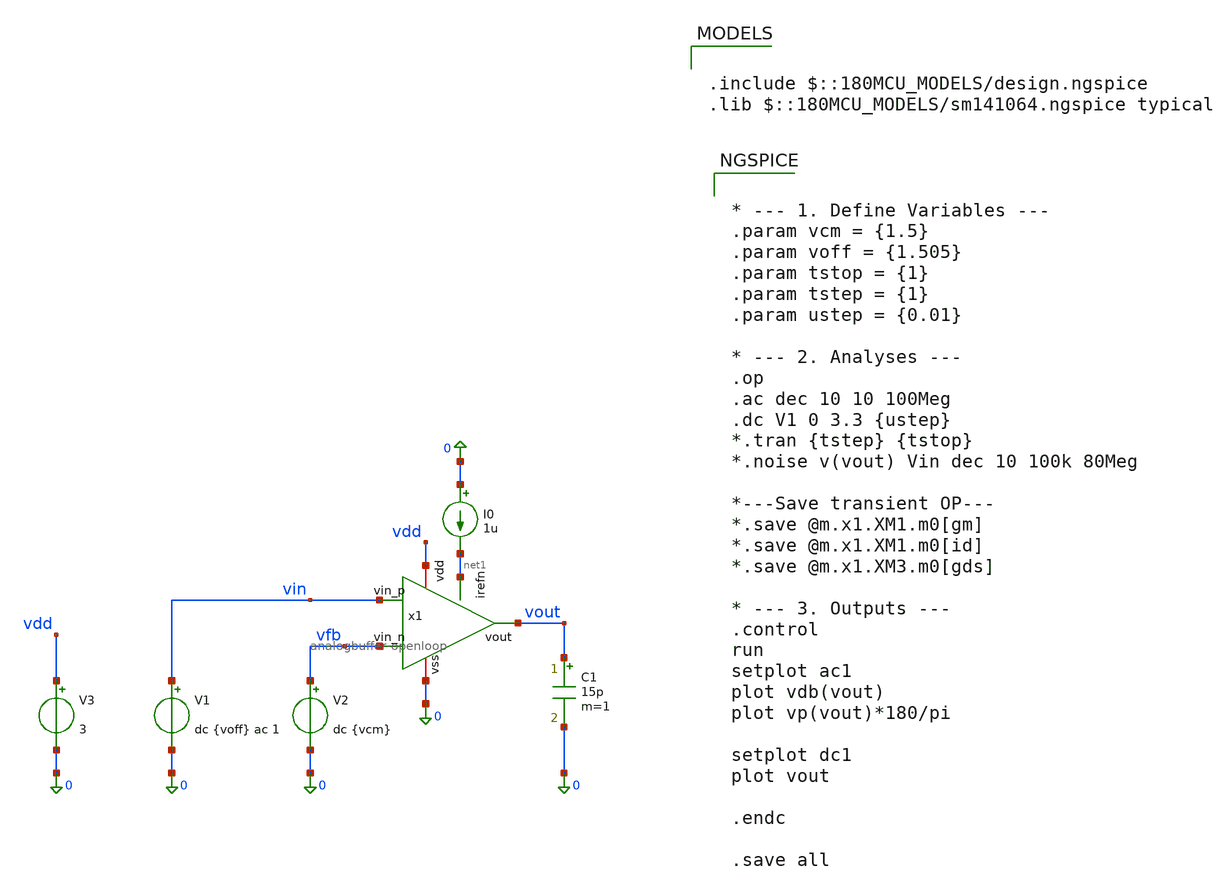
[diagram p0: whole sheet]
** sch_path: Tobias/2026 07 17 Results/analogbuffer/analogbuffer-openloop-tb.sch
**.subckt analogbuffer-openloop-tb
x1 vdd net1 vin vout vfb 0 analogbuffer-openloop
V1 vin 0 dc {voff} ac 1
V2 vfb 0 dc {vcm}
C1 vout 0 15p m=1
I0 0 net1 1u
V3 vdd 0 3
**** begin user architecture code


* --- 1. Define Variables ---
.param vcm = {1.5}
.param voff = {1.505}
.param tstop = {1}
.param tstep = {1}
.param ustep = {0.01}

* --- 2. Analyses ---
.op
.ac dec 10 10 100Meg
.dc V1 0 3.3 {ustep}
*.tran {tstep} {tstop}
*.noise v(vout) Vin dec 10 100k 80Meg

*---Save transient OP---
*.save @m.x1.XM1.m0[gm]
*.save @m.x1.XM1.m0[id]
*.save @m.x1.XM3.m0[gds]

* --- 3. Outputs ---
.control
run
setplot ac1
plot vdb(vout)
plot vp(vout)*180/pi

setplot dc1
plot vout

.endc

.save all



.include $::180MCU_MODELS/design.ngspice
.lib $::180MCU_MODELS/sm141064.ngspice typical

**** end user architecture code
**.ends

* expanding   symbol:  analogbuffer/analogbuffer-openloop.sym # of pins=6
** sym_path: Tobias/2026 07 17 Results/analogbuffer/analogbuffer-openloop.sym
** sch_path: Tobias/2026 07 17 Results/analogbuffer/analogbuffer-openloop.sch
.subckt analogbuffer-openloop vdd irefn vin_p vout vin_n vss
*.iopin vdd
*.iopin vss
*.ipin vin_p
*.opin vout
*.ipin irefn
*.ipin vin_n
XM2P net7 vin_p net10 vdd pfet_03v3 L=4u W=80u nf=1 ad='int((nf+1)/2) * W/nf * 0.18u' as='int((nf+2)/2) * W/nf * 0.18u'
+ pd='2*int((nf+1)/2) * (W/nf + 0.18u)' ps='2*int((nf+2)/2) * (W/nf + 0.18u)' nrd='0.18u / W' nrs='0.18u / W'
+ sa=0 sb=0 sd=0 m=1
XM2N net1 vin_p net4 vss nfet_03v3 L=4u W=40u nf=1 ad='int((nf+1)/2) * W/nf * 0.18u' as='int((nf+2)/2) * W/nf * 0.18u'
+ pd='2*int((nf+1)/2) * (W/nf + 0.18u)' ps='2*int((nf+2)/2) * (W/nf + 0.18u)' nrd='0.18u / W' nrs='0.18u / W'
+ sa=0 sb=0 sd=0 m=1
XM3N net4 net8 vss vss nfet_03v3 L=4u W=2u nf=1 ad='int((nf+1)/2) * W/nf * 0.18u' as='int((nf+2)/2) * W/nf * 0.18u'
+ pd='2*int((nf+1)/2) * (W/nf + 0.18u)' ps='2*int((nf+2)/2) * (W/nf + 0.18u)' nrd='0.18u / W' nrs='0.18u / W'
+ sa=0 sb=0 sd=0 m=1
XM1NR net3 vin_n net4 vss nfet_03v3 L=4u W=40u nf=1 ad='int((nf+1)/2) * W/nf * 0.18u' as='int((nf+2)/2) * W/nf * 0.18u'
+ pd='2*int((nf+1)/2) * (W/nf + 0.18u)' ps='2*int((nf+2)/2) * (W/nf + 0.18u)' nrd='0.18u / W' nrs='0.18u / W'
+ sa=0 sb=0 sd=0 m=1
XM2NR net3 net3 vdd vdd pfet_03v3 L=2u W=4u nf=1 ad='int((nf+1)/2) * W/nf * 0.18u' as='int((nf+2)/2) * W/nf * 0.18u'
+ pd='2*int((nf+1)/2) * (W/nf + 0.18u)' ps='2*int((nf+2)/2) * (W/nf + 0.18u)' nrd='0.18u / W' nrs='0.18u / W'
+ sa=0 sb=0 sd=0 m=1
XM3NR net2 net3 vdd vdd pfet_03v3 L=2u W=4u nf=1 ad='int((nf+1)/2) * W/nf * 0.18u' as='int((nf+2)/2) * W/nf * 0.18u'
+ pd='2*int((nf+1)/2) * (W/nf + 0.18u)' ps='2*int((nf+2)/2) * (W/nf + 0.18u)' nrd='0.18u / W' nrs='0.18u / W'
+ sa=0 sb=0 sd=0 m=1
XM4NR net2 net2 vdd vdd pfet_03v3 L=2u W=4u nf=1 ad='int((nf+1)/2) * W/nf * 0.18u' as='int((nf+2)/2) * W/nf * 0.18u'
+ pd='2*int((nf+1)/2) * (W/nf + 0.18u)' ps='2*int((nf+2)/2) * (W/nf + 0.18u)' nrd='0.18u / W' nrs='0.18u / W'
+ sa=0 sb=0 sd=0 m=1
XM5NR vout net2 vdd vdd pfet_03v3 L=2u W=40u nf=1 ad='int((nf+1)/2) * W/nf * 0.18u' as='int((nf+2)/2) * W/nf * 0.18u'
+ pd='2*int((nf+1)/2) * (W/nf + 0.18u)' ps='2*int((nf+2)/2) * (W/nf + 0.18u)' nrd='0.18u / W' nrs='0.18u / W'
+ sa=0 sb=0 sd=0 m=1
XM5N vout net1 vdd vdd pfet_03v3 L=2u W=40u nf=1 ad='int((nf+1)/2) * W/nf * 0.18u' as='int((nf+2)/2) * W/nf * 0.18u'
+ pd='2*int((nf+1)/2) * (W/nf + 0.18u)' ps='2*int((nf+2)/2) * (W/nf + 0.18u)' nrd='0.18u / W' nrs='0.18u / W'
+ sa=0 sb=0 sd=0 m=1
XM4N net1 net1 vdd vdd pfet_03v3 L=2u W=4u nf=1 ad='int((nf+1)/2) * W/nf * 0.18u' as='int((nf+2)/2) * W/nf * 0.18u'
+ pd='2*int((nf+1)/2) * (W/nf + 0.18u)' ps='2*int((nf+2)/2) * (W/nf + 0.18u)' nrd='0.18u / W' nrs='0.18u / W'
+ sa=0 sb=0 sd=0 m=1
XM5NS net2 irefn vss vss nfet_03v3 L=2u W=2u nf=1 ad='int((nf+1)/2) * W/nf * 0.18u' as='int((nf+2)/2) * W/nf * 0.18u'
+ pd='2*int((nf+1)/2) * (W/nf + 0.18u)' ps='2*int((nf+2)/2) * (W/nf + 0.18u)' nrd='0.18u / W' nrs='0.18u / W'
+ sa=0 sb=0 sd=0 m=1
XM1PR net5 vin_n net10 vdd pfet_03v3 L=4u W=80u nf=1 ad='int((nf+1)/2) * W/nf * 0.18u' as='int((nf+2)/2) * W/nf * 0.18u'
+ pd='2*int((nf+1)/2) * (W/nf + 0.18u)' ps='2*int((nf+2)/2) * (W/nf + 0.18u)' nrd='0.18u / W' nrs='0.18u / W'
+ sa=0 sb=0 sd=0 m=1
XM3P net10 net9 vdd vdd pfet_03v3 L=4u W=4u nf=1 ad='int((nf+1)/2) * W/nf * 0.18u' as='int((nf+2)/2) * W/nf * 0.18u'
+ pd='2*int((nf+1)/2) * (W/nf + 0.18u)' ps='2*int((nf+2)/2) * (W/nf + 0.18u)' nrd='0.18u / W' nrs='0.18u / W'
+ sa=0 sb=0 sd=0 m=1
XM2PR net5 net5 vss vss nfet_03v3 L=2u W=2u nf=1 ad='int((nf+1)/2) * W/nf * 0.18u' as='int((nf+2)/2) * W/nf * 0.18u'
+ pd='2*int((nf+1)/2) * (W/nf + 0.18u)' ps='2*int((nf+2)/2) * (W/nf + 0.18u)' nrd='0.18u / W' nrs='0.18u / W'
+ sa=0 sb=0 sd=0 m=1
XM3PR net6 net5 vss vss nfet_03v3 L=2u W=2u nf=1 ad='int((nf+1)/2) * W/nf * 0.18u' as='int((nf+2)/2) * W/nf * 0.18u'
+ pd='2*int((nf+1)/2) * (W/nf + 0.18u)' ps='2*int((nf+2)/2) * (W/nf + 0.18u)' nrd='0.18u / W' nrs='0.18u / W'
+ sa=0 sb=0 sd=0 m=1
XM4PR net6 net6 vss vss nfet_03v3 L=2u W=2u nf=1 ad='int((nf+1)/2) * W/nf * 0.18u' as='int((nf+2)/2) * W/nf * 0.18u'
+ pd='2*int((nf+1)/2) * (W/nf + 0.18u)' ps='2*int((nf+2)/2) * (W/nf + 0.18u)' nrd='0.18u / W' nrs='0.18u / W'
+ sa=0 sb=0 sd=0 m=1
XM5PR vout net6 vss vss nfet_03v3 L=2u W=20u nf=1 ad='int((nf+1)/2) * W/nf * 0.18u' as='int((nf+2)/2) * W/nf * 0.18u'
+ pd='2*int((nf+1)/2) * (W/nf + 0.18u)' ps='2*int((nf+2)/2) * (W/nf + 0.18u)' nrd='0.18u / W' nrs='0.18u / W'
+ sa=0 sb=0 sd=0 m=1
XM5PS net6 irefp vdd vdd pfet_03v3 L=2u W=4u nf=1 ad='int((nf+1)/2) * W/nf * 0.18u' as='int((nf+2)/2) * W/nf * 0.18u'
+ pd='2*int((nf+1)/2) * (W/nf + 0.18u)' ps='2*int((nf+2)/2) * (W/nf + 0.18u)' nrd='0.18u / W' nrs='0.18u / W'
+ sa=0 sb=0 sd=0 m=1
XM5P vout net7 vss vss nfet_03v3 L=2u W=20u nf=1 ad='int((nf+1)/2) * W/nf * 0.18u' as='int((nf+2)/2) * W/nf * 0.18u'
+ pd='2*int((nf+1)/2) * (W/nf + 0.18u)' ps='2*int((nf+2)/2) * (W/nf + 0.18u)' nrd='0.18u / W' nrs='0.18u / W'
+ sa=0 sb=0 sd=0 m=1
XM4P net7 net7 vss vss nfet_03v3 L=2u W=2u nf=1 ad='int((nf+1)/2) * W/nf * 0.18u' as='int((nf+2)/2) * W/nf * 0.18u'
+ pd='2*int((nf+1)/2) * (W/nf + 0.18u)' ps='2*int((nf+2)/2) * (W/nf + 0.18u)' nrd='0.18u / W' nrs='0.18u / W'
+ sa=0 sb=0 sd=0 m=1
XM2NS irefp irefn vss vss nfet_03v3 L=2u W=1u nf=1 ad='int((nf+1)/2) * W/nf * 0.18u' as='int((nf+2)/2) * W/nf * 0.18u'
+ pd='2*int((nf+1)/2) * (W/nf + 0.18u)' ps='2*int((nf+2)/2) * (W/nf + 0.18u)' nrd='0.18u / W' nrs='0.18u / W'
+ sa=0 sb=0 sd=0 m=1
XM1NS irefn irefn vss vss nfet_03v3 L=2u W=1u nf=1 ad='int((nf+1)/2) * W/nf * 0.18u' as='int((nf+2)/2) * W/nf * 0.18u'
+ pd='2*int((nf+1)/2) * (W/nf + 0.18u)' ps='2*int((nf+2)/2) * (W/nf + 0.18u)' nrd='0.18u / W' nrs='0.18u / W'
+ sa=0 sb=0 sd=0 m=1
XM2PS irefp irefp vdd vdd pfet_03v3 L=2u W=2u nf=1 ad='int((nf+1)/2) * W/nf * 0.18u' as='int((nf+2)/2) * W/nf * 0.18u'
+ pd='2*int((nf+1)/2) * (W/nf + 0.18u)' ps='2*int((nf+2)/2) * (W/nf + 0.18u)' nrd='0.18u / W' nrs='0.18u / W'
+ sa=0 sb=0 sd=0 m=1
XMSN vdd net11 net8 vss nfet_03v3 L=2u W=2u nf=1 ad='int((nf+1)/2) * W/nf * 0.18u' as='int((nf+2)/2) * W/nf * 0.18u'
+ pd='2*int((nf+1)/2) * (W/nf + 0.18u)' ps='2*int((nf+2)/2) * (W/nf + 0.18u)' nrd='0.18u / W' nrs='0.18u / W'
+ sa=0 sb=0 sd=0 m=1
XM3NS net8 irefn vss vss nfet_03v3 L=2u W=2u nf=1 ad='int((nf+1)/2) * W/nf * 0.18u' as='int((nf+2)/2) * W/nf * 0.18u'
+ pd='2*int((nf+1)/2) * (W/nf + 0.18u)' ps='2*int((nf+2)/2) * (W/nf + 0.18u)' nrd='0.18u / W' nrs='0.18u / W'
+ sa=0 sb=0 sd=0 m=1
XM1N net11 vin_n net4 vss nfet_03v3 L=4u W=40u nf=1 ad='int((nf+1)/2) * W/nf * 0.18u' as='int((nf+2)/2) * W/nf * 0.18u'
+ pd='2*int((nf+1)/2) * (W/nf + 0.18u)' ps='2*int((nf+2)/2) * (W/nf + 0.18u)' nrd='0.18u / W' nrs='0.18u / W'
+ sa=0 sb=0 sd=0 m=1
XM4PS net11 irefp vdd vdd pfet_03v3 L=2u W=4u nf=1 ad='int((nf+1)/2) * W/nf * 0.18u' as='int((nf+2)/2) * W/nf * 0.18u'
+ pd='2*int((nf+1)/2) * (W/nf + 0.18u)' ps='2*int((nf+2)/2) * (W/nf + 0.18u)' nrd='0.18u / W' nrs='0.18u / W'
+ sa=0 sb=0 sd=0 m=1
XM3PS net9 irefp vdd vdd pfet_03v3 L=2u W=4u nf=1 ad='int((nf+1)/2) * W/nf * 0.18u' as='int((nf+2)/2) * W/nf * 0.18u'
+ pd='2*int((nf+1)/2) * (W/nf + 0.18u)' ps='2*int((nf+2)/2) * (W/nf + 0.18u)' nrd='0.18u / W' nrs='0.18u / W'
+ sa=0 sb=0 sd=0 m=1
XM1P net12 vin_n net10 vdd pfet_03v3 L=4u W=80u nf=1 ad='int((nf+1)/2) * W/nf * 0.18u' as='int((nf+2)/2) * W/nf * 0.18u'
+ pd='2*int((nf+1)/2) * (W/nf + 0.18u)' ps='2*int((nf+2)/2) * (W/nf + 0.18u)' nrd='0.18u / W' nrs='0.18u / W'
+ sa=0 sb=0 sd=0 m=1
XM4NS net12 irefn vss vss nfet_03v3 L=2u W=2u nf=1 ad='int((nf+1)/2) * W/nf * 0.18u' as='int((nf+2)/2) * W/nf * 0.18u'
+ pd='2*int((nf+1)/2) * (W/nf + 0.18u)' ps='2*int((nf+2)/2) * (W/nf + 0.18u)' nrd='0.18u / W' nrs='0.18u / W'
+ sa=0 sb=0 sd=0 m=1
XMSP vss net12 net9 vdd pfet_03v3 L=1u W=4u nf=1 ad='int((nf+1)/2) * W/nf * 0.18u' as='int((nf+2)/2) * W/nf * 0.18u'
+ pd='2*int((nf+1)/2) * (W/nf + 0.18u)' ps='2*int((nf+2)/2) * (W/nf + 0.18u)' nrd='0.18u / W' nrs='0.18u / W'
+ sa=0 sb=0 sd=0 m=1
.ends

.end
